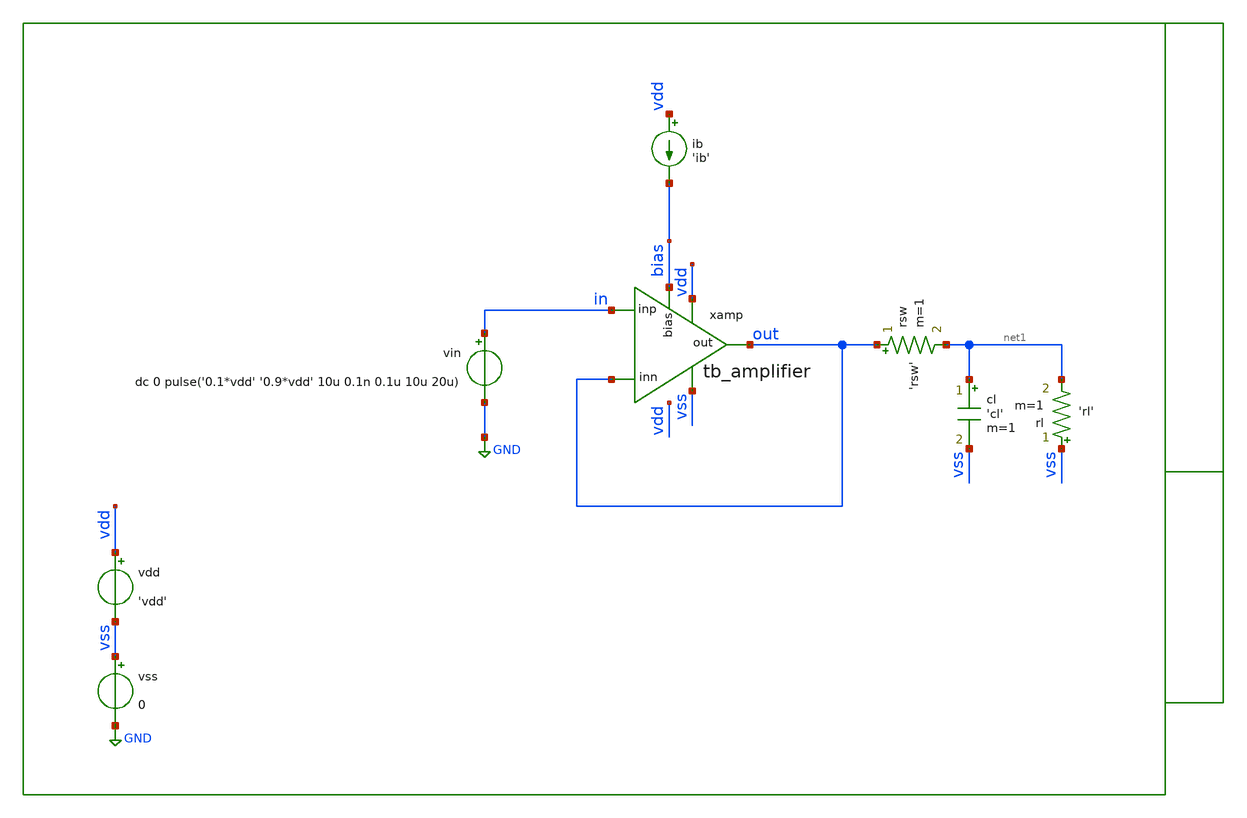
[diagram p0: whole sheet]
** sch_path: xschem/tb/testbuffer/tb_amplifier/tr_tb_amplifier_slew.sch
**.subckt tr_tb_amplifier_slew
ib vdd bias 'ib'
cl net1 vss 'cl' m=1
vin in GND dc 0 pulse('0.1*vdd' '0.9*vdd' 10u 0.1n 0.1u 10u 20u)
rl vss net1 'rl' m=1
vdd vdd vss 'vdd'
vss vss GND 0
xamp vdd out in out vss bias tb_amplifier
rsw out net1 'rsw' m=1
**** begin user architecture code
 * Control

.param vdd=3.3
.param vcm='vdd/2'
.param ib=5u
.param cl=10p
.param rl=1e6
.param rsw=1

.control
save all

tran 100n 60u uic


meas tran vsupply find v(vdd) at=1u

let vmeas_max=vsupply/2+0.2
let vmeas_min=vsupply/2-0.2


meas tran td_pos TRIG v(out) VAL=vmeas_min RISE=2 TARG v(out) VAL=vmeas_max RISE=2
meas tran td_neg TRIG v(out) VAL=vmeas_max FALL=2 TARG v(out) VAL=vmeas_min FALL=2

let sr_pos=(vmeas_max-vmeas_min)/td_pos
let sr_neg=(vmeas_max-vmeas_min)/td_neg

print sr_pos
print sr_neg

set wr_singlescale
set wr_vecnames
wrdata data.csv out

.endc

 * Model Corners

.include $::CORNERS/ngspice/tt.spice
*.include $::CORNERS/ngspice/ff.spice
*.include $::CORNERS/ngspice/ss.spice
*.include $::CORNERS/ngspice/sf.spice
*.include $::CORNERS/ngspice/fs.spice

**** end user architecture code
**.ends

* expanding   symbol:  sch/testbuffer/tb_amplifier/tb_amplifier.sym # of pins=6
** sym_path: xschem/sch/testbuffer/tb_amplifier/tb_amplifier.sym
** sch_path: xschem/sch/testbuffer/tb_amplifier/tb_amplifier.sch
.subckt tb_amplifier vdd out inp inn vss bias
*.ipin inn
*.ipin inp
*.opin out
*.iopin bias
*.iopin vdd
*.iopin vss
XM3 mirr mirr vdd vdd pfet_06v0 L=4u W=16u nf=2 ad='int((nf+1)/2) * W/nf * 0.18u' as='int((nf+2)/2) * W/nf * 0.18u'
+ pd='2*int((nf+1)/2) * (W/nf + 0.18u)' ps='2*int((nf+2)/2) * (W/nf + 0.18u)' nrd='0.18u / W' nrs='0.18u / W'
+ sa=0 sb=0 sd=0 m=2 par=2
XM4 comp mirr vdd vdd pfet_06v0 L=4u W=16u nf=2 ad='int((nf+1)/2) * W/nf * 0.18u' as='int((nf+2)/2) * W/nf * 0.18u'
+ pd='2*int((nf+1)/2) * (W/nf + 0.18u)' ps='2*int((nf+2)/2) * (W/nf + 0.18u)' nrd='0.18u / W' nrs='0.18u / W'
+ sa=0 sb=0 sd=0 m=2 par=2
XM2 comp inp vcm vss nfet_06v0 L=2u W=16u nf=2 ad='int((nf+1)/2) * W/nf * 0.18u' as='int((nf+2)/2) * W/nf * 0.18u'
+ pd='2*int((nf+1)/2) * (W/nf + 0.18u)' ps='2*int((nf+2)/2) * (W/nf + 0.18u)' nrd='0.18u / W' nrs='0.18u / W'
+ sa=0 sb=0 sd=0 m=2 par=2
XM1 mirr inn vcm vss nfet_06v0 L=2u W=16u nf=2 ad='int((nf+1)/2) * W/nf * 0.18u' as='int((nf+2)/2) * W/nf * 0.18u'
+ pd='2*int((nf+1)/2) * (W/nf + 0.18u)' ps='2*int((nf+2)/2) * (W/nf + 0.18u)' nrd='0.18u / W' nrs='0.18u / W'
+ sa=0 sb=0 sd=0 m=2 par=2
XM5 vcm bias vss vss nfet_06v0 L=1u W=16u nf=2 ad='int((nf+1)/2) * W/nf * 0.18u' as='int((nf+2)/2) * W/nf * 0.18u'
+ pd='2*int((nf+1)/2) * (W/nf + 0.18u)' ps='2*int((nf+2)/2) * (W/nf + 0.18u)' nrd='0.18u / W' nrs='0.18u / W'
+ sa=0 sb=0 sd=0 m=2 par=2
XM6 out bias vss vss nfet_06v0 L=1u W=16u nf=2 ad='int((nf+1)/2) * W/nf * 0.18u' as='int((nf+2)/2) * W/nf * 0.18u'
+ pd='2*int((nf+1)/2) * (W/nf + 0.18u)' ps='2*int((nf+2)/2) * (W/nf + 0.18u)' nrd='0.18u / W' nrs='0.18u / W'
+ sa=0 sb=0 sd=0 m=12 par=12
XM7 out comp vdd vdd pfet_06v0 L=1u W=96u nf=12 ad='int((nf+1)/2) * W/nf * 0.18u' as='int((nf+2)/2) * W/nf * 0.18u'
+ pd='2*int((nf+1)/2) * (W/nf + 0.18u)' ps='2*int((nf+2)/2) * (W/nf + 0.18u)' nrd='0.18u / W' nrs='0.18u / W'
+ sa=0 sb=0 sd=0 m=1 par=1
XMB1 bias bias vss vss nfet_06v0 L=1u W=16u nf=2 ad='int((nf+1)/2) * W/nf * 0.18u' as='int((nf+2)/2) * W/nf * 0.18u'
+ pd='2*int((nf+1)/2) * (W/nf + 0.18u)' ps='2*int((nf+2)/2) * (W/nf + 0.18u)' nrd='0.18u / W' nrs='0.18u / W'
+ sa=0 sb=0 sd=0 m=2 par=2
XMB2 vbm bias vss vss nfet_06v0 L=1u W=16u nf=2 ad='int((nf+1)/2) * W/nf * 0.18u' as='int((nf+2)/2) * W/nf * 0.18u'
+ pd='2*int((nf+1)/2) * (W/nf + 0.18u)' ps='2*int((nf+2)/2) * (W/nf + 0.18u)' nrd='0.18u / W' nrs='0.18u / W'
+ sa=0 sb=0 sd=0 m=2 par=2
XMB3 vbm vbm vbt vdd pfet_06v0 L=1u W=16u nf=2 ad='int((nf+1)/2) * W/nf * 0.18u' as='int((nf+2)/2) * W/nf * 0.18u'
+ pd='2*int((nf+1)/2) * (W/nf + 0.18u)' ps='2*int((nf+2)/2) * (W/nf + 0.18u)' nrd='0.18u / W' nrs='0.18u / W'
+ sa=0 sb=0 sd=0 m=1 par=1
XMB4 vbt vbt vdd vdd pfet_06v0 L=1u W=16u nf=2 ad='int((nf+1)/2) * W/nf * 0.18u' as='int((nf+2)/2) * W/nf * 0.18u'
+ pd='2*int((nf+1)/2) * (W/nf + 0.18u)' ps='2*int((nf+2)/2) * (W/nf + 0.18u)' nrd='0.18u / W' nrs='0.18u / W'
+ sa=0 sb=0 sd=0 m=1 par=1
XRCC gc comp vdd ppolyf_u_1k_6p0 r_width=2e-6 r_length=38e-6 s=1 m=1
XMDUM1 vss vss vss vss nfet_06v0 L=2u W=16u nf=2 ad='int((nf+1)/2) * W/nf * 0.18u' as='int((nf+2)/2) * W/nf * 0.18u'
+ pd='2*int((nf+1)/2) * (W/nf + 0.18u)' ps='2*int((nf+2)/2) * (W/nf + 0.18u)' nrd='0.18u / W' nrs='0.18u / W'
+ sa=0 sb=0 sd=0 m=2 par=2
XMDUM2 vdd vdd vdd vdd pfet_06v0 L=4u W=16u nf=2 ad='int((nf+1)/2) * W/nf * 0.18u' as='int((nf+2)/2) * W/nf * 0.18u'
+ pd='2*int((nf+1)/2) * (W/nf + 0.18u)' ps='2*int((nf+2)/2) * (W/nf + 0.18u)' nrd='0.18u / W' nrs='0.18u / W'
+ sa=0 sb=0 sd=0 m=4 par=4
XC1 out gc cap_mim_2f0_m4m5_noshield c_width=30e-6 c_length=30e-6 m=1
.ends

.GLOBAL GND
.end
